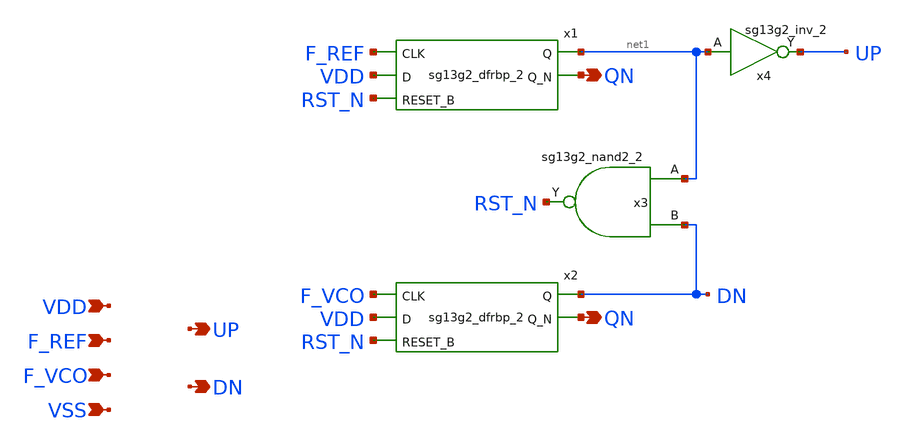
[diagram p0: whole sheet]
** sch_path: schematic/blocks/phase-freq-detector/PFD_std.sch
* IHP-GmbH/IHP-Open-PDK/ihp-sg13g2/libs.tech/xschem/sg13g2_stdcells/sg13g2_inv_2.sch:
* Copyright 2023 IHP PDK Authors
* Licensed under the Apache License, Version 2.0 (the "License");
**.subckt PFD_std UP F_REF VDD VSS DN F_VCO QN QN
*.opin UP
*.ipin F_REF
*.ipin VDD
*.ipin VSS
*.opin DN
*.ipin F_VCO
*.opin QN
*.opin QN
x1 net1 QN F_REF VDD RST_N VDD GND sg13g2_dfrbp_2
x2 DN QN F_VCO VDD RST_N VDD GND sg13g2_dfrbp_2
x3 RST_N net1 DN VDD GND sg13g2_nand2_2
x4 UP net1 VDD GND sg13g2_inv_2
**.ends

* expanding   symbol:  sg13g2_stdcells/sg13g2_dfrbp_2.sym # of pins=5
** sym_path: sg13g2_stdcells/sg13g2_dfrbp_2.sym
** sch_path: sg13g2_stdcells/sg13g2_dfrbp_2.sch
.subckt sg13g2_dfrbp_2 Q Q_N CLK D RESET_B VDD VSS
*.ipin D
*.ipin RESET_B
*.ipin CLK
*.opin Q
*.opin Q_N
*.iopin VDD
*.iopin VSS
XM1 Db D net12 VSS sg13_lv_nmos w=420.00n l=130.00n ng=1 m=1 mm_ok=1
XM2 net12 RESET_B VSS VSS sg13_lv_nmos w=420.00n l=130.00n ng=1 m=1 mm_ok=1
XM3 net2 clkneg net11 VSS sg13_lv_nmos w=420.00n l=130.00n ng=1 m=1 mm_ok=1
XM4 net11 net3 VSS VSS sg13_lv_nmos w=420.00n l=130.00n ng=1 m=1 mm_ok=1
XM5 net3 net2 net7 VSS sg13_lv_nmos w=420.00n l=130.00n ng=1 m=1 mm_ok=1
XM6 net7 RESET_B VSS VSS sg13_lv_nmos w=420.00n l=130.00n ng=1 m=1 mm_ok=1
XM7 Q_N net2 VSS VSS sg13_lv_nmos w=1.48u l=130.00n ng=2 m=1 mm_ok=1
XM8 net1 net2 VSS VSS sg13_lv_nmos w=640.00n l=130.00n ng=1 m=1 mm_ok=1
XM9 Q net1 VSS VSS sg13_lv_nmos w=1.48u l=130.00n ng=2 m=1 mm_ok=1
XM10 clkneg CLK VSS VSS sg13_lv_nmos w=740.00n l=130.00n ng=1 m=1 mm_ok=1
XM11 clkpos clkneg VSS VSS sg13_lv_nmos w=740.00n l=130.00n ng=1 m=1 mm_ok=1
XM12 Db clkneg net4 VSS sg13_lv_nmos w=420.00n l=130.00n ng=1 m=1 mm_ok=1
XM13 net4 clkpos net10 VSS sg13_lv_nmos w=420.00n l=130.00n ng=1 m=1 mm_ok=1
XM14 net10 net5 net6 VSS sg13_lv_nmos w=420.00n l=130.00n ng=1 m=1 mm_ok=1
XM15 net6 RESET_B VSS VSS sg13_lv_nmos w=420.00n l=130.00n ng=1 m=1 mm_ok=1
XM16 net5 net4 VSS VSS sg13_lv_nmos w=740.00n l=130.00n ng=1 m=1 mm_ok=1
XM17 net5 clkpos net2 VSS sg13_lv_nmos w=740.00n l=130.00n ng=1 m=1 mm_ok=1
XM18 Db RESET_B VDD VDD sg13_lv_pmos w=420.00n l=130.00n ng=1 m=1 mm_ok=1
XM19 Db D VDD VDD sg13_lv_pmos w=420.00n l=130.00n ng=1 m=1 mm_ok=1
XM20 net9 net3 VDD VDD sg13_lv_pmos w=420.00n l=130.00n ng=1 m=1 mm_ok=1
XM21 net2 clkpos net9 VDD sg13_lv_pmos w=420.00n l=130.00n ng=1 m=1 mm_ok=1
XM22 net3 net2 VDD VDD sg13_lv_pmos w=420.00n l=130.00n ng=1 m=1 mm_ok=1
XM23 net3 RESET_B VDD VDD sg13_lv_pmos w=420.00n l=130.00n ng=1 m=1 mm_ok=1
XM24 Q_N net2 VDD VDD sg13_lv_pmos w=2.24u l=130.00n ng=2 m=1 mm_ok=1
XM25 net1 net2 VDD VDD sg13_lv_pmos w=1.000u l=130.00n ng=1 m=1 mm_ok=1
XM26 Q net1 VDD VDD sg13_lv_pmos w=2.24u l=130.00n ng=2 m=1 mm_ok=1
XM27 clkneg CLK VDD VDD sg13_lv_pmos w=1.12u l=130.00n ng=1 m=1 mm_ok=1
XM28 clkpos clkneg VDD VDD sg13_lv_pmos w=1.12u l=130.00n ng=1 m=1 mm_ok=1
XM29 Db clkpos net4 VDD sg13_lv_pmos w=420.00n l=130.00n ng=1 m=1 mm_ok=1
XM30 net8 net5 VDD VDD sg13_lv_pmos w=420.00n l=130.00n ng=1 m=1 mm_ok=1
XM31 net4 clkneg net8 VDD sg13_lv_pmos w=420.00n l=130.00n ng=1 m=1 mm_ok=1
XM32 net4 RESET_B VDD VDD sg13_lv_pmos w=420.00n l=130.00n ng=1 m=1 mm_ok=1
XM33 net5 net4 VDD VDD sg13_lv_pmos w=1.000u l=130.00n ng=1 m=1 mm_ok=1
XM34 net5 clkneg net2 VDD sg13_lv_pmos w=1.000u l=130.00n ng=1 m=1 mm_ok=1
.ends


* expanding   symbol:  sg13g2_stdcells/sg13g2_nand2_2.sym # of pins=3
** sym_path: sg13g2_stdcells/sg13g2_nand2_2.sym
** sch_path: sg13g2_stdcells/sg13g2_nand2_2.sch
.subckt sg13g2_nand2_2 Y A B VDD VSS
*.iopin VDD
*.iopin VSS
*.opin Y
*.ipin B
*.ipin A
XM1 Y A net1 VSS sg13_lv_nmos w=1.44u l=130.00n ng=2 m=1 mm_ok=1
XM2 net1 B VSS VSS sg13_lv_nmos w=1.44u l=130.00n ng=2 m=1 mm_ok=1
XM3 Y A VDD VDD sg13_lv_pmos w=2.24u l=130.00n ng=2 m=1 mm_ok=1
XM4 Y B VDD VDD sg13_lv_pmos w=2.24u l=130.00n ng=2 m=1 mm_ok=1
.ends


* expanding   symbol:  sg13g2_stdcells/sg13g2_inv_2.sym # of pins=2
** sym_path: sg13g2_stdcells/sg13g2_inv_2.sym
** sch_path: sg13g2_stdcells/sg13g2_inv_2.sch
.subckt sg13g2_inv_2 Y A VDD VSS
*.opin Y
*.ipin A
*.iopin VDD
*.iopin VSS
XM1 Y A VSS VSS sg13_lv_nmos w=1.48u l=130.00n ng=2 m=1 mm_ok=1
XM2 Y A VDD VDD sg13_lv_pmos w=2.24u l=130.00n ng=2 m=1 mm_ok=1
.ends

.end
